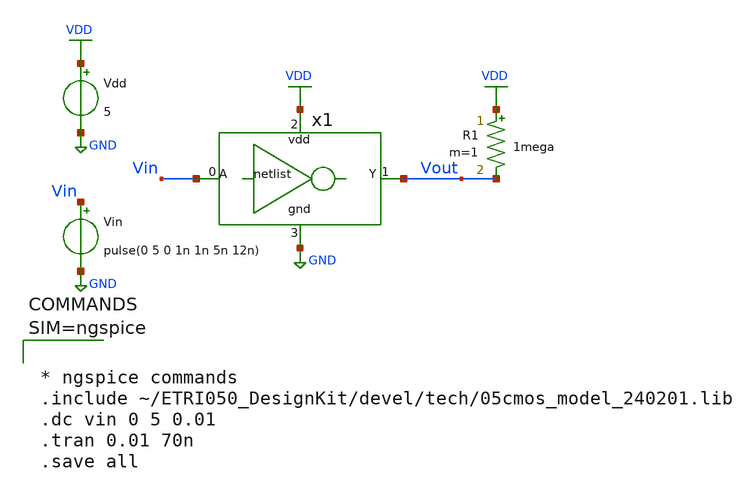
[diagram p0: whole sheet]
** sch_path: Tutorials/1-2_Inverter_Magic/inverter_x1_TB.sch
**.subckt inverter_x1_TB
Vdd VDD GND 5
R1 VDD Vout 1mega m=1
Vin Vin GND pulse(0 5 0 1n 1n 5n 12n)
x1 Vin Vout VDD GND inverter_x1
**** begin user architecture code



* ngspice commands
.include ~/ETRI050_DesignKit/devel/tech/05cmos_model_240201.lib
.dc vin 0 5 0.01
.tran 0.01 70n
.save all



**** end user architecture code
**.ends

* expanding   symbol:  /home/goodkook/ETRI050_DesignKit/Tutorials/1-2_Inverter_Magic/inverter_x1.sym
*+ # of pins=4
** sym_path: Tutorials/1-2_Inverter_Magic/inverter_x1.sym
.include ~/ETRI050_DesignKit/Tutorials/1-2_Inverter_Magic/inverter_x1.spice
.GLOBAL VDD
.GLOBAL GND
.end
